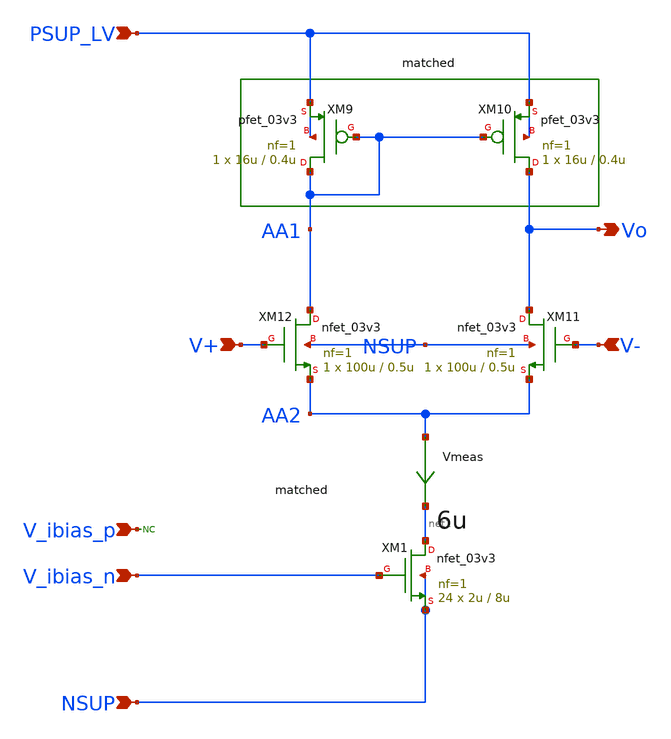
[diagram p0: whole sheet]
** sch_path: xschem/blocks/aux_amp/aux_amp.sch
**.subckt aux_amp PSUP_LV NSUP V+ V- V_ibias_n V_ibias_p Vo
*.ipin PSUP_LV
*.ipin NSUP
*.ipin V+
*.ipin V-
*.ipin V_ibias_n
*.ipin V_ibias_p
*.opin Vo
XM9 AA1 AA1 PSUP_LV PSUP_LV pfet_03v3 L=0.4u W=16u nf=1 ad='int((nf+1)/2) * W/nf * 0.18u' as='int((nf+2)/2) * W/nf * 0.18u'
+ pd='2*int((nf+1)/2) * (W/nf + 0.18u)' ps='2*int((nf+2)/2) * (W/nf + 0.18u)' nrd='0.18u / W' nrs='0.18u / W'
+ sa=0 sb=0 sd=0 m=1
XM10 Vo AA1 PSUP_LV PSUP_LV pfet_03v3 L=0.4u W=16u nf=1 ad='int((nf+1)/2) * W/nf * 0.18u' as='int((nf+2)/2) * W/nf * 0.18u'
+ pd='2*int((nf+1)/2) * (W/nf + 0.18u)' ps='2*int((nf+2)/2) * (W/nf + 0.18u)' nrd='0.18u / W' nrs='0.18u / W'
+ sa=0 sb=0 sd=0 m=1
XM11 Vo V- AA2 NSUP nfet_03v3 L=0.5u W=100u nf=1 ad='int((nf+1)/2) * W/nf * 0.18u' as='int((nf+2)/2) * W/nf * 0.18u'
+ pd='2*int((nf+1)/2) * (W/nf + 0.18u)' ps='2*int((nf+2)/2) * (W/nf + 0.18u)' nrd='0.18u / W' nrs='0.18u / W'
+ sa=0 sb=0 sd=0 m=1
XM12 AA1 V+ AA2 NSUP nfet_03v3 L=0.5u W=100u nf=1 ad='int((nf+1)/2) * W/nf * 0.18u' as='int((nf+2)/2) * W/nf * 0.18u'
+ pd='2*int((nf+1)/2) * (W/nf + 0.18u)' ps='2*int((nf+2)/2) * (W/nf + 0.18u)' nrd='0.18u / W' nrs='0.18u / W'
+ sa=0 sb=0 sd=0 m=1
XM1 net1 V_ibias_n NSUP NSUP nfet_03v3 L=8u W=2u nf=1 ad='int((nf+1)/2) * W/nf * 0.18u' as='int((nf+2)/2) * W/nf * 0.18u'
+ pd='2*int((nf+1)/2) * (W/nf + 0.18u)' ps='2*int((nf+2)/2) * (W/nf + 0.18u)' nrd='0.18u / W' nrs='0.18u / W'
+ sa=0 sb=0 sd=0 m=24
Vmeas AA2 net1 0
.save i(vmeas)
* noconn V_ibias_p
**.ends
.end
